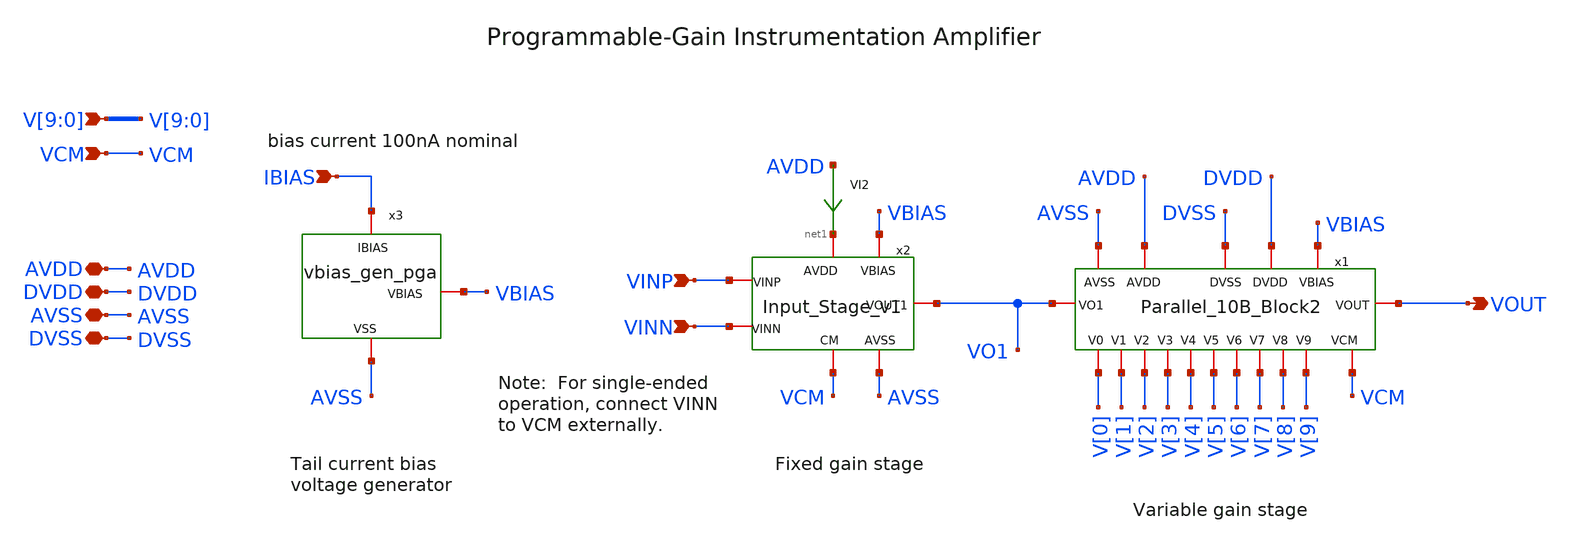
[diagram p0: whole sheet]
** sch_path: xschem/sky130_pa_ip__instramp.sch
**.subckt sky130_pa_ip__instramp VCM AVDD VOUT IBIAS DVDD AVSS DVSS
*+ V[9],V[8],V[7],V[6],V[5],V[4],V[3],V[2],V[1],V[0] VINP VINN
*.ipin VCM
*.iopin AVDD
*.opin VOUT
*.ipin IBIAS
*.iopin DVDD
*.iopin AVSS
*.iopin DVSS
*.ipin V[9],V[8],V[7],V[6],V[5],V[4],V[3],V[2],V[1],V[0]
*.ipin VINP
*.ipin VINN
x1 V[6] V[5] V[8] V[9] V[7] VO1 DVDD AVDD VOUT V[4] V[3] V[2] V[1] V[0] VCM DVSS AVSS VBIAS
+ Parallel_10B_Block2
x2 net1 VINP VO1 VINN VCM AVSS VBIAS Input_Stage_v1
VI2 AVDD net1 0
.save i(vi2)
x3 VBIAS IBIAS AVSS vbias_gen_pga
**.ends
.end
